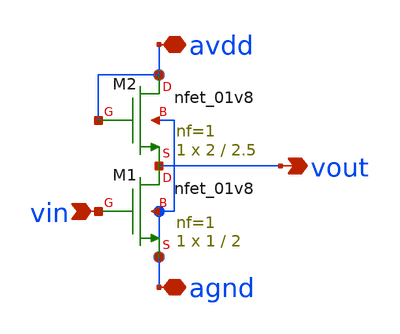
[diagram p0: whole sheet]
** sch_path: AMP_Old/Final_Amp_Diode.sch
**.subckt Final_Amp_Diode avdd vin vout agnd
*.iopin avdd
*.ipin vin
*.opin vout
*.iopin agnd
XM1 vout vin agnd agnd sky130_fd_pr__nfet_01v8 L=2 W=1 nf=1 ad='int((nf+1)/2) * W/nf * 0.29' as='int((nf+2)/2) * W/nf * 0.29'
+ pd='2*int((nf+1)/2) * (W/nf + 0.29)' ps='2*int((nf+2)/2) * (W/nf + 0.29)' nrd='0.29 / W' nrs='0.29 / W'
+ sa=0 sb=0 sd=0 mult=1 m=1
XM2 avdd avdd vout agnd sky130_fd_pr__nfet_01v8 L=2.5 W=2 nf=1 ad='int((nf+1)/2) * W/nf * 0.29' as='int((nf+2)/2) * W/nf * 0.29'
+ pd='2*int((nf+1)/2) * (W/nf + 0.29)' ps='2*int((nf+2)/2) * (W/nf + 0.29)' nrd='0.29 / W' nrs='0.29 / W'
+ sa=0 sb=0 sd=0 mult=1 m=1
**.ends
.end
